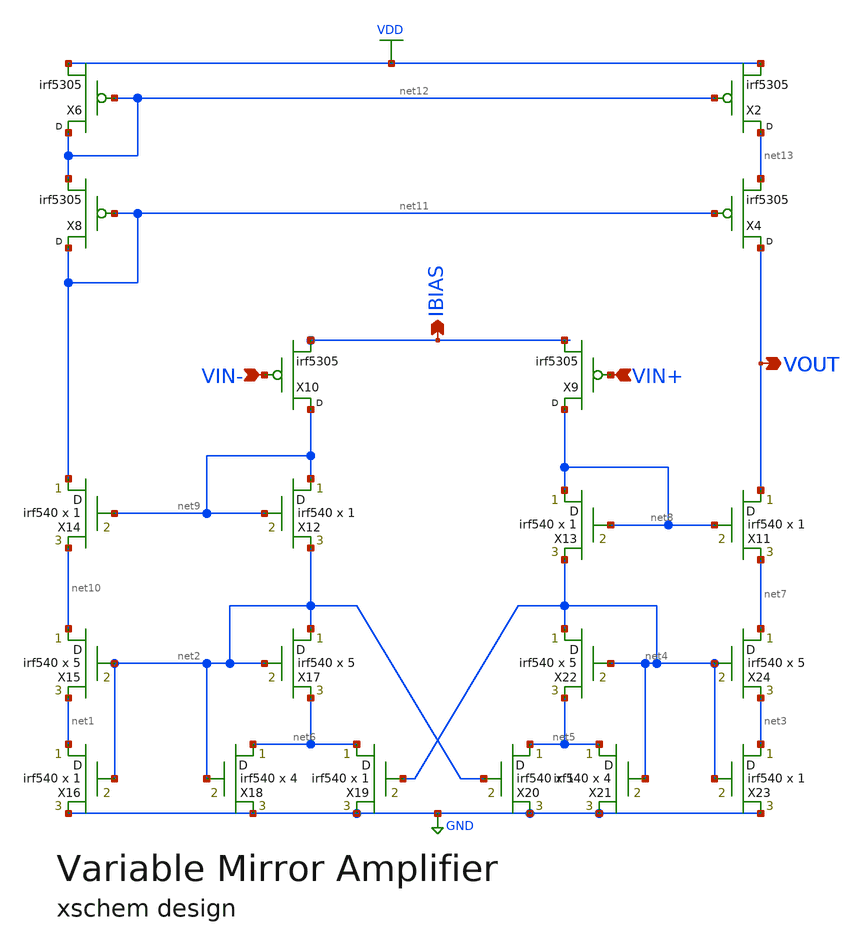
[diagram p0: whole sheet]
** sch_path: VMA.sch
**.subckt VMA VIN+ VIN- VOUT IBIAS VOUT VOUT
*.ipin VIN+
*.ipin VIN-
*.opin VOUT
*.opin IBIAS
*.opin VOUT
*.opin VOUT
X2 net13 net12 VDD irf5305
X4 VOUT net11 net13 irf5305
X6 net12 net12 VDD irf5305
X8 net11 net11 net12 irf5305
X9 net8 VIN+ IBIAS irf5305
X10 net9 VIN- IBIAS irf5305
X11 VOUT net8 net7 irf540 m=1
X12 net9 net9 net2 irf540 m=1
X13 net8 net8 net4 irf540 m=1
X14 net11 net9 net10 irf540 m=1
X15 net10 net2 net1 irf540 m=5
X16 net1 net2 GND irf540 m=1
X17 net2 net2 net6 irf540 m=5
X18 net6 net2 GND irf540 m=4
X19 net6 net4 GND irf540 m=1
X20 net5 net2 GND irf540 m=1
X21 net5 net4 GND irf540 m=4
X22 net4 net4 net5 irf540 m=5
X23 net3 net4 GND irf540 m=1
X24 net7 net4 net3 irf540 m=5
**.ends
.GLOBAL VDD
.GLOBAL GND
.end
